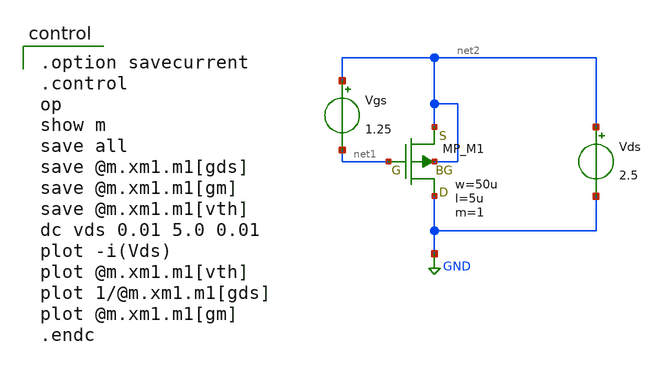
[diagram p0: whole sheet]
** sch_path: member_project/opamp/cat_nekonekone/meas_gm-rds-vth/pmos_idvds.sch
**.subckt pmos_idvds
Vgs net2 net1 1.25
Vds net2 GND 2.5
XM1 GND net1 net2 net2 PMOS w=50u l=5u as=0 ad=0 ps=0 pd=0 nrd=0 nrs=0 m=1
**** begin user architecture code

.option savecurrent
.control
op
show m
save all
save @m.xm1.m1[gds]
save @m.xm1.m1[gm]
save @m.xm1.m1[vth]
dc vds 0.01 5.0 0.01
plot -i(Vds)
plot @m.xm1.m1[vth]
plot 1/@m.xm1.m1[gds]
plot @m.xm1.m1[gm]
.endc

 .include $::LIB/ip62_models
**** end user architecture code
**.ends
.GLOBAL GND
.end
